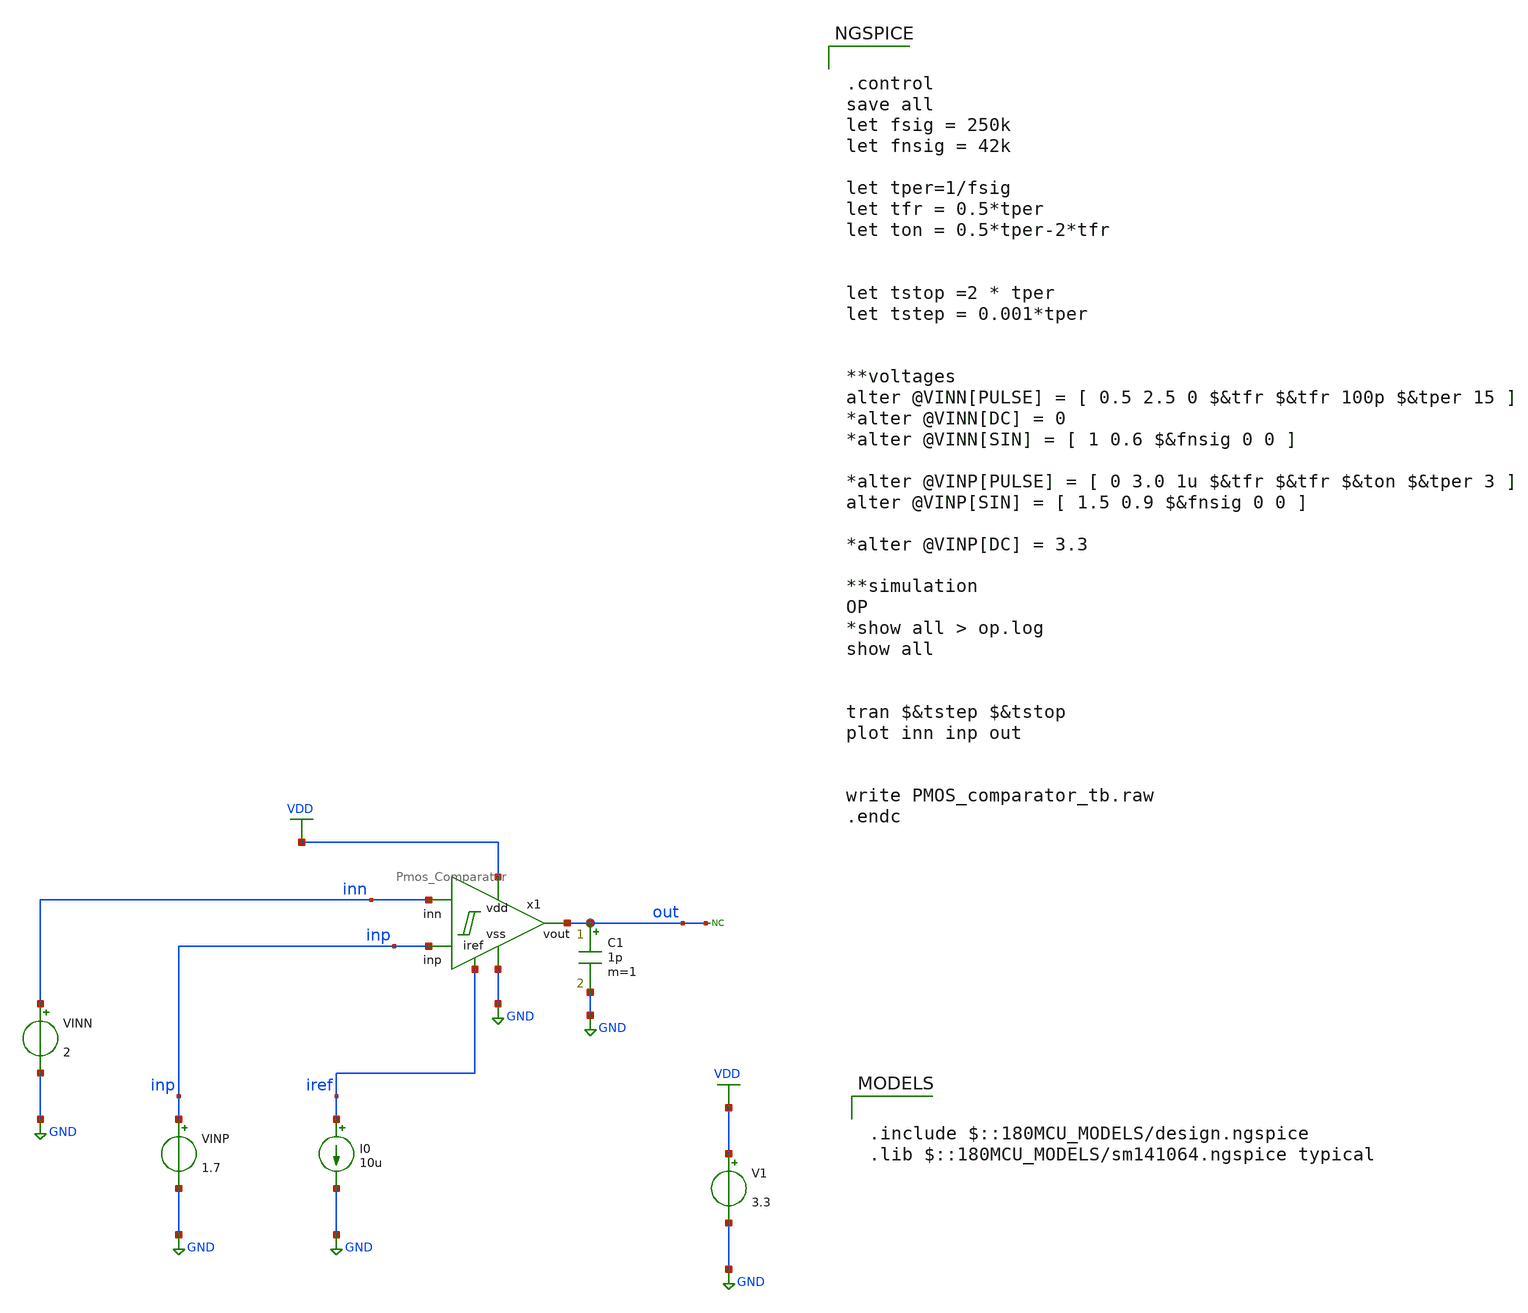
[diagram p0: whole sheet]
** sch_path: designs/libs/tb_analog/Comparator/PMOS_comparator_tb.sch
**.subckt PMOS_comparator_tb
I0 iref GND 10u
V1 VDD GND 3.3
VINP inp GND 1.7
C1 out GND 1p m=1
* noconn out
VINN inn GND 2
x1 VDD out inp GND inn iref Pmos_Comparator
**** begin user architecture code


.control
save all
let fsig = 250k
let fnsig = 42k

let tper=1/fsig
let tfr = 0.5*tper
let ton = 0.5*tper-2*tfr


let tstop =2 * tper
let tstep = 0.001*tper


**voltages
alter @VINN[PULSE] = [ 0.5 2.5 0 $&tfr $&tfr 100p $&tper 15 ]
*alter @VINN[DC] = 0
*alter @VINN[SIN] = [ 1 0.6 $&fnsig 0 0 ]

*alter @VINP[PULSE] = [ 0 3.0 1u $&tfr $&tfr $&ton $&tper 3 ]
alter @VINP[SIN] = [ 1.5 0.9 $&fnsig 0 0 ]

*alter @VINP[DC] = 3.3

**simulation
OP
*show all > op.log
show all


tran $&tstep $&tstop
plot inn inp out


write PMOS_comparator_tb.raw
.endc



.include $::180MCU_MODELS/design.ngspice
.lib $::180MCU_MODELS/sm141064.ngspice typical

**** end user architecture code
**.ends
.GLOBAL GND
.GLOBAL VDD
.end
